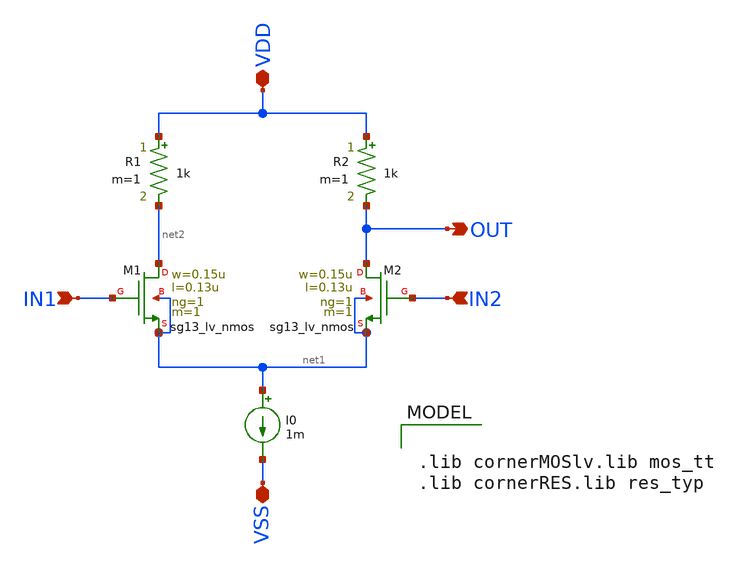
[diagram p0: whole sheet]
** sch_path: xschem/diff_pair.sch
**.subckt diff_pair VDD VSS IN1 IN2 OUT
*.iopin VDD
*.iopin VSS
*.ipin IN1
*.ipin IN2
*.opin OUT
XM1 net2 IN1 net1 net1 sg13_lv_nmos w=0.15u l=0.13u ng=1 m=1 mm_ok=1
XM2 OUT IN2 net1 net1 sg13_lv_nmos w=0.15u l=0.13u ng=1 m=1 mm_ok=1
I0 net1 VSS 1m
R1 VDD net2 1k m=1
R2 VDD OUT 1k m=1
**** begin user architecture code


.lib cornerMOSlv.lib mos_tt
.lib cornerRES.lib res_typ


**** end user architecture code
**.ends
.end
